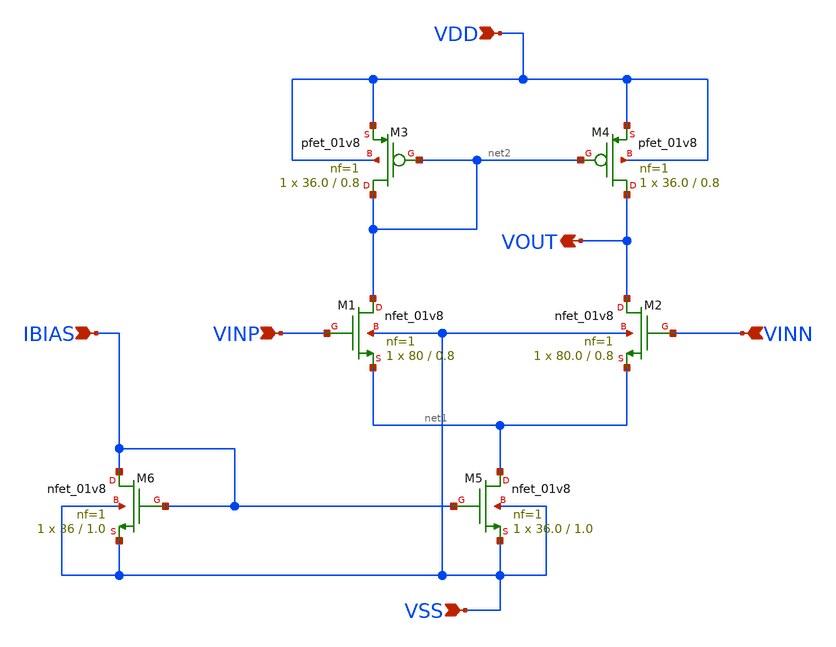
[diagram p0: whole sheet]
** sch_path: lelo_5tota_sky130a/design/LELO_5TOTA_SKY130A/LELO_5TOTA.sch
**.subckt LELO_5TOTA VDD VSS VOUT IBIAS VINP VINN
*.ipin VDD
*.ipin VSS
*.opin VOUT
*.ipin IBIAS
*.ipin VINP
*.ipin VINN
XM2 VOUT VINN net1 VSS sky130_fd_pr__nfet_01v8 L=0.8 W=80.0 nf=1 ad='int((1 + 1)/2) * 80.0 / 1 * 0.29'
+ as='int((1 + 2)/2) * 80.0 / 1 * 0.29' pd='2*int((1 + 1)/2) * (80.0 / 1 + 0.29)' ps='2*int((1 + 2)/2) * (80.0 / 1 + 0.29)'
+ nrd='0.29 / 80.0 ' nrs='0.29 / 80.0 ' sa=0 sb=0 sd=0 mult=1 m=1
XM4 VOUT net2 VDD VDD sky130_fd_pr__pfet_01v8 L=0.8 W=36.0 nf=1 ad='int((1 + 1)/2) * 36.0 / 1 * 0.29'
+ as='int((1 + 2)/2) * 36.0 / 1 * 0.29' pd='2*int((1 + 1)/2) * (36.0 / 1 + 0.29)' ps='2*int((1 + 2)/2) * (36.0 / 1 + 0.29)'
+ nrd='0.29 / 36.0 ' nrs='0.29 / 36.0 ' sa=0 sb=0 sd=0 mult=1 m=1
XM3 net2 net2 VDD VDD sky130_fd_pr__pfet_01v8 L=0.8 W=36.0 nf=1 ad='int((1 + 1)/2) * 36.0 / 1 * 0.29'
+ as='int((1 + 2)/2) * 36.0 / 1 * 0.29' pd='2*int((1 + 1)/2) * (36.0 / 1 + 0.29)' ps='2*int((1 + 2)/2) * (36.0 / 1 + 0.29)'
+ nrd='0.29 / 36.0 ' nrs='0.29 / 36.0 ' sa=0 sb=0 sd=0 mult=1 m=1
XM6 IBIAS IBIAS VSS VSS sky130_fd_pr__nfet_01v8 L=1.0 W=36 nf=1 ad='int((1 + 1)/2) * 36 / 1 * 0.29' as='int((1 + 2)/2) * 36 / 1 * 0.29'
+ pd='2*int((1 + 1)/2) * (36 / 1 + 0.29)' ps='2*int((1 + 2)/2) * (36 / 1 + 0.29)' nrd='0.29 / 36 ' nrs='0.29 / 36 '
+ sa=0 sb=0 sd=0 mult=1 m=1
XM1 net2 VINP net1 VSS sky130_fd_pr__nfet_01v8 L=0.8 W=80 nf=1 ad='int((1 + 1)/2) * 80 / 1 * 0.29' as='int((1 + 2)/2) * 80 / 1 * 0.29'
+ pd='2*int((1 + 1)/2) * (80 / 1 + 0.29)' ps='2*int((1 + 2)/2) * (80 / 1 + 0.29)' nrd='0.29 / 80 ' nrs='0.29 / 80 '
+ sa=0 sb=0 sd=0 mult=1 m=1
XM5 net1 IBIAS VSS VSS sky130_fd_pr__nfet_01v8 L=1.0 W=36.0 nf=1 ad='int((1 + 1)/2) * 36.0 / 1 * 0.29'
+ as='int((1 + 2)/2) * 36.0 / 1 * 0.29' pd='2*int((1 + 1)/2) * (36.0 / 1 + 0.29)' ps='2*int((1 + 2)/2) * (36.0 / 1 + 0.29)'
+ nrd='0.29 / 36.0 ' nrs='0.29 / 36.0 ' sa=0 sb=0 sd=0 mult=1 m=1
**.ends
.end
